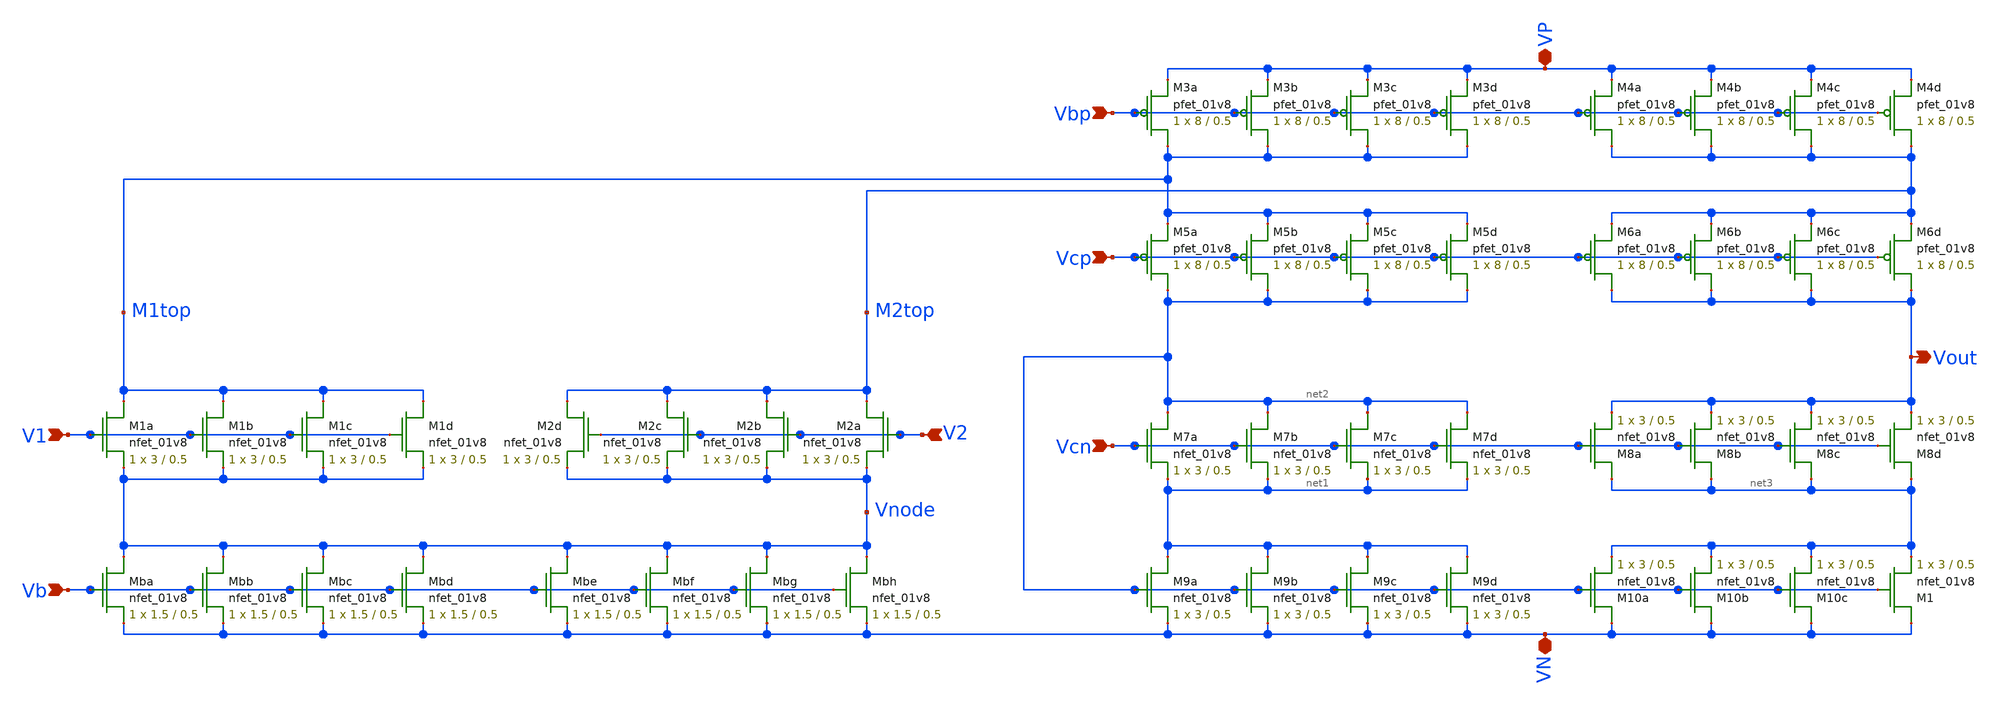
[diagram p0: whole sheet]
** sch_path: xschem/other_project_files/opamp_schematic_balanced.sch
**.subckt opamp_schematic_balanced Vbp Vcp Vcn V2 V1 Vb VP VN Vout
*.ipin Vbp
*.ipin Vcp
*.ipin Vcn
*.ipin V2
*.ipin V1
*.ipin Vb
*.iopin VP
*.iopin VN
*.opin Vout
XM1a M1top V1 Vnode GND sky130_fd_pr__nfet_01v8 L=0.5 W=3 nf=1 ad='int((nf+1)/2) * W/nf * 0.29' as='int((nf+2)/2) * W/nf * 0.29'
+ pd='2*int((nf+1)/2) * (W/nf + 0.29)' ps='2*int((nf+2)/2) * (W/nf + 0.29)' nrd='0.29 / W' nrs='0.29 / W'
+ sa=0 sb=0 sd=0 mult=1 m=1
XM1b M1top V1 Vnode GND sky130_fd_pr__nfet_01v8 L=0.5 W=3 nf=1 ad='int((nf+1)/2) * W/nf * 0.29' as='int((nf+2)/2) * W/nf * 0.29'
+ pd='2*int((nf+1)/2) * (W/nf + 0.29)' ps='2*int((nf+2)/2) * (W/nf + 0.29)' nrd='0.29 / W' nrs='0.29 / W'
+ sa=0 sb=0 sd=0 mult=1 m=1
XM1c M1top V1 Vnode GND sky130_fd_pr__nfet_01v8 L=0.5 W=3 nf=1 ad='int((nf+1)/2) * W/nf * 0.29' as='int((nf+2)/2) * W/nf * 0.29'
+ pd='2*int((nf+1)/2) * (W/nf + 0.29)' ps='2*int((nf+2)/2) * (W/nf + 0.29)' nrd='0.29 / W' nrs='0.29 / W'
+ sa=0 sb=0 sd=0 mult=1 m=1
XM1d M1top V1 Vnode GND sky130_fd_pr__nfet_01v8 L=0.5 W=3 nf=1 ad='int((nf+1)/2) * W/nf * 0.29' as='int((nf+2)/2) * W/nf * 0.29'
+ pd='2*int((nf+1)/2) * (W/nf + 0.29)' ps='2*int((nf+2)/2) * (W/nf + 0.29)' nrd='0.29 / W' nrs='0.29 / W'
+ sa=0 sb=0 sd=0 mult=1 m=1
XM2a M2top V2 Vnode GND sky130_fd_pr__nfet_01v8 L=0.5 W=3 nf=1 ad='int((nf+1)/2) * W/nf * 0.29' as='int((nf+2)/2) * W/nf * 0.29'
+ pd='2*int((nf+1)/2) * (W/nf + 0.29)' ps='2*int((nf+2)/2) * (W/nf + 0.29)' nrd='0.29 / W' nrs='0.29 / W'
+ sa=0 sb=0 sd=0 mult=1 m=1
XM2b M2top V2 Vnode GND sky130_fd_pr__nfet_01v8 L=0.5 W=3 nf=1 ad='int((nf+1)/2) * W/nf * 0.29' as='int((nf+2)/2) * W/nf * 0.29'
+ pd='2*int((nf+1)/2) * (W/nf + 0.29)' ps='2*int((nf+2)/2) * (W/nf + 0.29)' nrd='0.29 / W' nrs='0.29 / W'
+ sa=0 sb=0 sd=0 mult=1 m=1
XM2c M2top V2 Vnode GND sky130_fd_pr__nfet_01v8 L=0.5 W=3 nf=1 ad='int((nf+1)/2) * W/nf * 0.29' as='int((nf+2)/2) * W/nf * 0.29'
+ pd='2*int((nf+1)/2) * (W/nf + 0.29)' ps='2*int((nf+2)/2) * (W/nf + 0.29)' nrd='0.29 / W' nrs='0.29 / W'
+ sa=0 sb=0 sd=0 mult=1 m=1
XM2d M2top V2 Vnode GND sky130_fd_pr__nfet_01v8 L=0.5 W=3 nf=1 ad='int((nf+1)/2) * W/nf * 0.29' as='int((nf+2)/2) * W/nf * 0.29'
+ pd='2*int((nf+1)/2) * (W/nf + 0.29)' ps='2*int((nf+2)/2) * (W/nf + 0.29)' nrd='0.29 / W' nrs='0.29 / W'
+ sa=0 sb=0 sd=0 mult=1 m=1
XMba Vnode Vb VN GND sky130_fd_pr__nfet_01v8 L=0.5 W=1.5 nf=1 ad='int((nf+1)/2) * W/nf * 0.29' as='int((nf+2)/2) * W/nf * 0.29'
+ pd='2*int((nf+1)/2) * (W/nf + 0.29)' ps='2*int((nf+2)/2) * (W/nf + 0.29)' nrd='0.29 / W' nrs='0.29 / W'
+ sa=0 sb=0 sd=0 mult=1 m=1
XMbb Vnode Vb VN GND sky130_fd_pr__nfet_01v8 L=0.5 W=1.5 nf=1 ad='int((nf+1)/2) * W/nf * 0.29' as='int((nf+2)/2) * W/nf * 0.29'
+ pd='2*int((nf+1)/2) * (W/nf + 0.29)' ps='2*int((nf+2)/2) * (W/nf + 0.29)' nrd='0.29 / W' nrs='0.29 / W'
+ sa=0 sb=0 sd=0 mult=1 m=1
XMbc Vnode Vb VN GND sky130_fd_pr__nfet_01v8 L=0.5 W=1.5 nf=1 ad='int((nf+1)/2) * W/nf * 0.29' as='int((nf+2)/2) * W/nf * 0.29'
+ pd='2*int((nf+1)/2) * (W/nf + 0.29)' ps='2*int((nf+2)/2) * (W/nf + 0.29)' nrd='0.29 / W' nrs='0.29 / W'
+ sa=0 sb=0 sd=0 mult=1 m=1
XMbd Vnode Vb VN GND sky130_fd_pr__nfet_01v8 L=0.5 W=1.5 nf=1 ad='int((nf+1)/2) * W/nf * 0.29' as='int((nf+2)/2) * W/nf * 0.29'
+ pd='2*int((nf+1)/2) * (W/nf + 0.29)' ps='2*int((nf+2)/2) * (W/nf + 0.29)' nrd='0.29 / W' nrs='0.29 / W'
+ sa=0 sb=0 sd=0 mult=1 m=1
XMbe Vnode Vb VN GND sky130_fd_pr__nfet_01v8 L=0.5 W=1.5 nf=1 ad='int((nf+1)/2) * W/nf * 0.29' as='int((nf+2)/2) * W/nf * 0.29'
+ pd='2*int((nf+1)/2) * (W/nf + 0.29)' ps='2*int((nf+2)/2) * (W/nf + 0.29)' nrd='0.29 / W' nrs='0.29 / W'
+ sa=0 sb=0 sd=0 mult=1 m=1
XMbf Vnode Vb VN GND sky130_fd_pr__nfet_01v8 L=0.5 W=1.5 nf=1 ad='int((nf+1)/2) * W/nf * 0.29' as='int((nf+2)/2) * W/nf * 0.29'
+ pd='2*int((nf+1)/2) * (W/nf + 0.29)' ps='2*int((nf+2)/2) * (W/nf + 0.29)' nrd='0.29 / W' nrs='0.29 / W'
+ sa=0 sb=0 sd=0 mult=1 m=1
XMbg Vnode Vb VN GND sky130_fd_pr__nfet_01v8 L=0.5 W=1.5 nf=1 ad='int((nf+1)/2) * W/nf * 0.29' as='int((nf+2)/2) * W/nf * 0.29'
+ pd='2*int((nf+1)/2) * (W/nf + 0.29)' ps='2*int((nf+2)/2) * (W/nf + 0.29)' nrd='0.29 / W' nrs='0.29 / W'
+ sa=0 sb=0 sd=0 mult=1 m=1
XMbh Vnode Vb VN GND sky130_fd_pr__nfet_01v8 L=0.5 W=1.5 nf=1 ad='int((nf+1)/2) * W/nf * 0.29' as='int((nf+2)/2) * W/nf * 0.29'
+ pd='2*int((nf+1)/2) * (W/nf + 0.29)' ps='2*int((nf+2)/2) * (W/nf + 0.29)' nrd='0.29 / W' nrs='0.29 / W'
+ sa=0 sb=0 sd=0 mult=1 m=1
XM7a net2 Vcn net1 GND sky130_fd_pr__nfet_01v8 L=0.5 W=3 nf=1 ad='int((nf+1)/2) * W/nf * 0.29' as='int((nf+2)/2) * W/nf * 0.29'
+ pd='2*int((nf+1)/2) * (W/nf + 0.29)' ps='2*int((nf+2)/2) * (W/nf + 0.29)' nrd='0.29 / W' nrs='0.29 / W'
+ sa=0 sb=0 sd=0 mult=1 m=1
XM7b net2 Vcn net1 GND sky130_fd_pr__nfet_01v8 L=0.5 W=3 nf=1 ad='int((nf+1)/2) * W/nf * 0.29' as='int((nf+2)/2) * W/nf * 0.29'
+ pd='2*int((nf+1)/2) * (W/nf + 0.29)' ps='2*int((nf+2)/2) * (W/nf + 0.29)' nrd='0.29 / W' nrs='0.29 / W'
+ sa=0 sb=0 sd=0 mult=1 m=1
XM7c net2 Vcn net1 GND sky130_fd_pr__nfet_01v8 L=0.5 W=3 nf=1 ad='int((nf+1)/2) * W/nf * 0.29' as='int((nf+2)/2) * W/nf * 0.29'
+ pd='2*int((nf+1)/2) * (W/nf + 0.29)' ps='2*int((nf+2)/2) * (W/nf + 0.29)' nrd='0.29 / W' nrs='0.29 / W'
+ sa=0 sb=0 sd=0 mult=1 m=1
XM7d net2 Vcn net1 GND sky130_fd_pr__nfet_01v8 L=0.5 W=3 nf=1 ad='int((nf+1)/2) * W/nf * 0.29' as='int((nf+2)/2) * W/nf * 0.29'
+ pd='2*int((nf+1)/2) * (W/nf + 0.29)' ps='2*int((nf+2)/2) * (W/nf + 0.29)' nrd='0.29 / W' nrs='0.29 / W'
+ sa=0 sb=0 sd=0 mult=1 m=1
XM8a net3 Vcn Vout GND sky130_fd_pr__nfet_01v8 L=0.5 W=3 nf=1 ad='int((nf+1)/2) * W/nf * 0.29' as='int((nf+2)/2) * W/nf * 0.29'
+ pd='2*int((nf+1)/2) * (W/nf + 0.29)' ps='2*int((nf+2)/2) * (W/nf + 0.29)' nrd='0.29 / W' nrs='0.29 / W'
+ sa=0 sb=0 sd=0 mult=1 m=1
XM8b net3 Vcn Vout GND sky130_fd_pr__nfet_01v8 L=0.5 W=3 nf=1 ad='int((nf+1)/2) * W/nf * 0.29' as='int((nf+2)/2) * W/nf * 0.29'
+ pd='2*int((nf+1)/2) * (W/nf + 0.29)' ps='2*int((nf+2)/2) * (W/nf + 0.29)' nrd='0.29 / W' nrs='0.29 / W'
+ sa=0 sb=0 sd=0 mult=1 m=1
XM8c net3 Vcn Vout GND sky130_fd_pr__nfet_01v8 L=0.5 W=3 nf=1 ad='int((nf+1)/2) * W/nf * 0.29' as='int((nf+2)/2) * W/nf * 0.29'
+ pd='2*int((nf+1)/2) * (W/nf + 0.29)' ps='2*int((nf+2)/2) * (W/nf + 0.29)' nrd='0.29 / W' nrs='0.29 / W'
+ sa=0 sb=0 sd=0 mult=1 m=1
XM8d net3 Vcn Vout GND sky130_fd_pr__nfet_01v8 L=0.5 W=3 nf=1 ad='int((nf+1)/2) * W/nf * 0.29' as='int((nf+2)/2) * W/nf * 0.29'
+ pd='2*int((nf+1)/2) * (W/nf + 0.29)' ps='2*int((nf+2)/2) * (W/nf + 0.29)' nrd='0.29 / W' nrs='0.29 / W'
+ sa=0 sb=0 sd=0 mult=1 m=1
XM9a net1 net2 VN GND sky130_fd_pr__nfet_01v8 L=0.5 W=3 nf=1 ad='int((nf+1)/2) * W/nf * 0.29' as='int((nf+2)/2) * W/nf * 0.29'
+ pd='2*int((nf+1)/2) * (W/nf + 0.29)' ps='2*int((nf+2)/2) * (W/nf + 0.29)' nrd='0.29 / W' nrs='0.29 / W'
+ sa=0 sb=0 sd=0 mult=1 m=1
XM9b net1 net2 VN GND sky130_fd_pr__nfet_01v8 L=0.5 W=3 nf=1 ad='int((nf+1)/2) * W/nf * 0.29' as='int((nf+2)/2) * W/nf * 0.29'
+ pd='2*int((nf+1)/2) * (W/nf + 0.29)' ps='2*int((nf+2)/2) * (W/nf + 0.29)' nrd='0.29 / W' nrs='0.29 / W'
+ sa=0 sb=0 sd=0 mult=1 m=1
XM9c net1 net2 VN GND sky130_fd_pr__nfet_01v8 L=0.5 W=3 nf=1 ad='int((nf+1)/2) * W/nf * 0.29' as='int((nf+2)/2) * W/nf * 0.29'
+ pd='2*int((nf+1)/2) * (W/nf + 0.29)' ps='2*int((nf+2)/2) * (W/nf + 0.29)' nrd='0.29 / W' nrs='0.29 / W'
+ sa=0 sb=0 sd=0 mult=1 m=1
XM9d net1 net2 VN GND sky130_fd_pr__nfet_01v8 L=0.5 W=3 nf=1 ad='int((nf+1)/2) * W/nf * 0.29' as='int((nf+2)/2) * W/nf * 0.29'
+ pd='2*int((nf+1)/2) * (W/nf + 0.29)' ps='2*int((nf+2)/2) * (W/nf + 0.29)' nrd='0.29 / W' nrs='0.29 / W'
+ sa=0 sb=0 sd=0 mult=1 m=1
XM10a VN net2 net3 GND sky130_fd_pr__nfet_01v8 L=0.5 W=3 nf=1 ad='int((nf+1)/2) * W/nf * 0.29' as='int((nf+2)/2) * W/nf * 0.29'
+ pd='2*int((nf+1)/2) * (W/nf + 0.29)' ps='2*int((nf+2)/2) * (W/nf + 0.29)' nrd='0.29 / W' nrs='0.29 / W'
+ sa=0 sb=0 sd=0 mult=1 m=1
XM10b VN net2 net3 GND sky130_fd_pr__nfet_01v8 L=0.5 W=3 nf=1 ad='int((nf+1)/2) * W/nf * 0.29' as='int((nf+2)/2) * W/nf * 0.29'
+ pd='2*int((nf+1)/2) * (W/nf + 0.29)' ps='2*int((nf+2)/2) * (W/nf + 0.29)' nrd='0.29 / W' nrs='0.29 / W'
+ sa=0 sb=0 sd=0 mult=1 m=1
XM10c VN net2 net3 GND sky130_fd_pr__nfet_01v8 L=0.5 W=3 nf=1 ad='int((nf+1)/2) * W/nf * 0.29' as='int((nf+2)/2) * W/nf * 0.29'
+ pd='2*int((nf+1)/2) * (W/nf + 0.29)' ps='2*int((nf+2)/2) * (W/nf + 0.29)' nrd='0.29 / W' nrs='0.29 / W'
+ sa=0 sb=0 sd=0 mult=1 m=1
XM1 VN net2 net3 GND sky130_fd_pr__nfet_01v8 L=0.5 W=3 nf=1 ad='int((nf+1)/2) * W/nf * 0.29' as='int((nf+2)/2) * W/nf * 0.29'
+ pd='2*int((nf+1)/2) * (W/nf + 0.29)' ps='2*int((nf+2)/2) * (W/nf + 0.29)' nrd='0.29 / W' nrs='0.29 / W'
+ sa=0 sb=0 sd=0 mult=1 m=1
XM5a net2 Vcp M1top VDD sky130_fd_pr__pfet_01v8 L=0.5 W=8 nf=1 ad='int((nf+1)/2) * W/nf * 0.29' as='int((nf+2)/2) * W/nf * 0.29'
+ pd='2*int((nf+1)/2) * (W/nf + 0.29)' ps='2*int((nf+2)/2) * (W/nf + 0.29)' nrd='0.29 / W' nrs='0.29 / W'
+ sa=0 sb=0 sd=0 mult=1 m=1
XM5b net2 Vcp M1top VDD sky130_fd_pr__pfet_01v8 L=0.5 W=8 nf=1 ad='int((nf+1)/2) * W/nf * 0.29' as='int((nf+2)/2) * W/nf * 0.29'
+ pd='2*int((nf+1)/2) * (W/nf + 0.29)' ps='2*int((nf+2)/2) * (W/nf + 0.29)' nrd='0.29 / W' nrs='0.29 / W'
+ sa=0 sb=0 sd=0 mult=1 m=1
XM5c net2 Vcp M1top VDD sky130_fd_pr__pfet_01v8 L=0.5 W=8 nf=1 ad='int((nf+1)/2) * W/nf * 0.29' as='int((nf+2)/2) * W/nf * 0.29'
+ pd='2*int((nf+1)/2) * (W/nf + 0.29)' ps='2*int((nf+2)/2) * (W/nf + 0.29)' nrd='0.29 / W' nrs='0.29 / W'
+ sa=0 sb=0 sd=0 mult=1 m=1
XM5d net2 Vcp M1top VDD sky130_fd_pr__pfet_01v8 L=0.5 W=8 nf=1 ad='int((nf+1)/2) * W/nf * 0.29' as='int((nf+2)/2) * W/nf * 0.29'
+ pd='2*int((nf+1)/2) * (W/nf + 0.29)' ps='2*int((nf+2)/2) * (W/nf + 0.29)' nrd='0.29 / W' nrs='0.29 / W'
+ sa=0 sb=0 sd=0 mult=1 m=1
XM6a Vout Vcp M2top VDD sky130_fd_pr__pfet_01v8 L=0.5 W=8 nf=1 ad='int((nf+1)/2) * W/nf * 0.29' as='int((nf+2)/2) * W/nf * 0.29'
+ pd='2*int((nf+1)/2) * (W/nf + 0.29)' ps='2*int((nf+2)/2) * (W/nf + 0.29)' nrd='0.29 / W' nrs='0.29 / W'
+ sa=0 sb=0 sd=0 mult=1 m=1
XM6b Vout Vcp M2top VDD sky130_fd_pr__pfet_01v8 L=0.5 W=8 nf=1 ad='int((nf+1)/2) * W/nf * 0.29' as='int((nf+2)/2) * W/nf * 0.29'
+ pd='2*int((nf+1)/2) * (W/nf + 0.29)' ps='2*int((nf+2)/2) * (W/nf + 0.29)' nrd='0.29 / W' nrs='0.29 / W'
+ sa=0 sb=0 sd=0 mult=1 m=1
XM6c Vout Vcp M2top VDD sky130_fd_pr__pfet_01v8 L=0.5 W=8 nf=1 ad='int((nf+1)/2) * W/nf * 0.29' as='int((nf+2)/2) * W/nf * 0.29'
+ pd='2*int((nf+1)/2) * (W/nf + 0.29)' ps='2*int((nf+2)/2) * (W/nf + 0.29)' nrd='0.29 / W' nrs='0.29 / W'
+ sa=0 sb=0 sd=0 mult=1 m=1
XM6d Vout Vcp M2top VDD sky130_fd_pr__pfet_01v8 L=0.5 W=8 nf=1 ad='int((nf+1)/2) * W/nf * 0.29' as='int((nf+2)/2) * W/nf * 0.29'
+ pd='2*int((nf+1)/2) * (W/nf + 0.29)' ps='2*int((nf+2)/2) * (W/nf + 0.29)' nrd='0.29 / W' nrs='0.29 / W'
+ sa=0 sb=0 sd=0 mult=1 m=1
XM3a M1top Vbp VP VDD sky130_fd_pr__pfet_01v8 L=0.5 W=8 nf=1 ad='int((nf+1)/2) * W/nf * 0.29' as='int((nf+2)/2) * W/nf * 0.29'
+ pd='2*int((nf+1)/2) * (W/nf + 0.29)' ps='2*int((nf+2)/2) * (W/nf + 0.29)' nrd='0.29 / W' nrs='0.29 / W'
+ sa=0 sb=0 sd=0 mult=1 m=1
XM3b M1top Vbp VP VDD sky130_fd_pr__pfet_01v8 L=0.5 W=8 nf=1 ad='int((nf+1)/2) * W/nf * 0.29' as='int((nf+2)/2) * W/nf * 0.29'
+ pd='2*int((nf+1)/2) * (W/nf + 0.29)' ps='2*int((nf+2)/2) * (W/nf + 0.29)' nrd='0.29 / W' nrs='0.29 / W'
+ sa=0 sb=0 sd=0 mult=1 m=1
XM3c M1top Vbp VP VDD sky130_fd_pr__pfet_01v8 L=0.5 W=8 nf=1 ad='int((nf+1)/2) * W/nf * 0.29' as='int((nf+2)/2) * W/nf * 0.29'
+ pd='2*int((nf+1)/2) * (W/nf + 0.29)' ps='2*int((nf+2)/2) * (W/nf + 0.29)' nrd='0.29 / W' nrs='0.29 / W'
+ sa=0 sb=0 sd=0 mult=1 m=1
XM3d M1top Vbp VP VDD sky130_fd_pr__pfet_01v8 L=0.5 W=8 nf=1 ad='int((nf+1)/2) * W/nf * 0.29' as='int((nf+2)/2) * W/nf * 0.29'
+ pd='2*int((nf+1)/2) * (W/nf + 0.29)' ps='2*int((nf+2)/2) * (W/nf + 0.29)' nrd='0.29 / W' nrs='0.29 / W'
+ sa=0 sb=0 sd=0 mult=1 m=1
XM4a M2top Vbp VP VDD sky130_fd_pr__pfet_01v8 L=0.5 W=8 nf=1 ad='int((nf+1)/2) * W/nf * 0.29' as='int((nf+2)/2) * W/nf * 0.29'
+ pd='2*int((nf+1)/2) * (W/nf + 0.29)' ps='2*int((nf+2)/2) * (W/nf + 0.29)' nrd='0.29 / W' nrs='0.29 / W'
+ sa=0 sb=0 sd=0 mult=1 m=1
XM4b M2top Vbp VP VDD sky130_fd_pr__pfet_01v8 L=0.5 W=8 nf=1 ad='int((nf+1)/2) * W/nf * 0.29' as='int((nf+2)/2) * W/nf * 0.29'
+ pd='2*int((nf+1)/2) * (W/nf + 0.29)' ps='2*int((nf+2)/2) * (W/nf + 0.29)' nrd='0.29 / W' nrs='0.29 / W'
+ sa=0 sb=0 sd=0 mult=1 m=1
XM4c M2top Vbp VP VDD sky130_fd_pr__pfet_01v8 L=0.5 W=8 nf=1 ad='int((nf+1)/2) * W/nf * 0.29' as='int((nf+2)/2) * W/nf * 0.29'
+ pd='2*int((nf+1)/2) * (W/nf + 0.29)' ps='2*int((nf+2)/2) * (W/nf + 0.29)' nrd='0.29 / W' nrs='0.29 / W'
+ sa=0 sb=0 sd=0 mult=1 m=1
XM4d M2top Vbp VP VDD sky130_fd_pr__pfet_01v8 L=0.5 W=8 nf=1 ad='int((nf+1)/2) * W/nf * 0.29' as='int((nf+2)/2) * W/nf * 0.29'
+ pd='2*int((nf+1)/2) * (W/nf + 0.29)' ps='2*int((nf+2)/2) * (W/nf + 0.29)' nrd='0.29 / W' nrs='0.29 / W'
+ sa=0 sb=0 sd=0 mult=1 m=1
**.ends
.end
